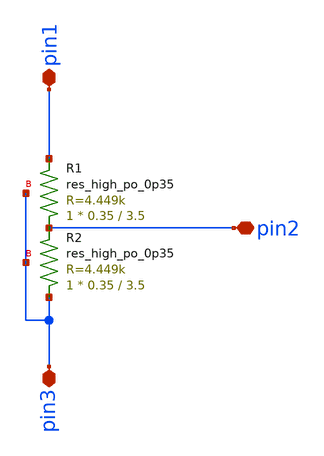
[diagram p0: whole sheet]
** sch_path: resistor_divider/xschem/resistor_divider.sch
**.subckt resistor_divider pin1 pin3 pin2
*.iopin pin1
*.iopin pin3
*.iopin pin2
XR1 pin2 pin1 pin3 sky130_fd_pr__res_high_po_0p35 L=3.5 mult=1 m=1
XR2 pin3 pin2 pin3 sky130_fd_pr__res_high_po_0p35 L=3.5 mult=1 m=1
**.ends
.end
